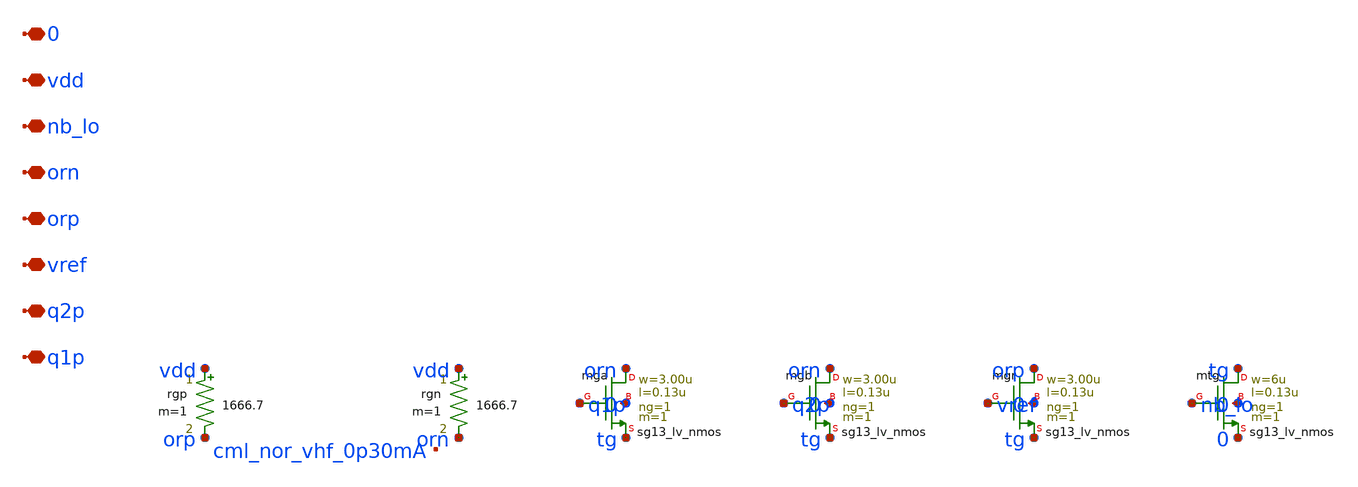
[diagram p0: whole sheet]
** sch_path: analog/lo/sch/cml_nor_vhf.sch
**.subckt cml_nor_vhf q1p q2p vref orp orn nb_lo vdd 0
*.iopin q1p
*.iopin q2p
*.iopin vref
*.iopin orp
*.iopin orn
*.iopin nb_lo
*.iopin vdd
*.iopin 0
rgp vdd orp 1666.7 m=1
rgn vdd orn 1666.7 m=1
Xmga orn q1p tg 0 sg13_lv_nmos w=3.00u l=0.13u ng=1 m=1 mm_ok=1
Xmgb orn q2p tg 0 sg13_lv_nmos w=3.00u l=0.13u ng=1 m=1 mm_ok=1
Xmgr orp vref tg 0 sg13_lv_nmos w=3.00u l=0.13u ng=1 m=1 mm_ok=1
Xmtg tg nb_lo 0 0 sg13_lv_nmos w=6u l=0.13u ng=1 m=1 mm_ok=1
**.ends
.end
